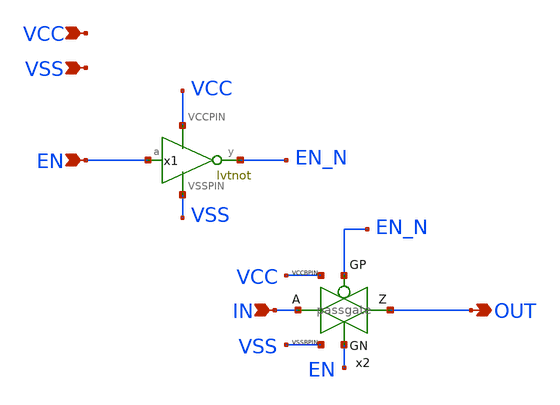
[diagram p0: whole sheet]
** sch_path: xschem/analogswitch.sch
* xschem/lvtnot.sym:
* Copyright 2021 Stefan Frederik Schippers
* Licensed under the Apache License, Version 2.0 (the "License");
**.subckt analogswitch EN IN OUT VCC VSS
*.ipin EN
*.ipin IN
*.opin OUT
*.ipin VCC
*.ipin VSS
x2 OUT IN EN_N EN VSS VCC passgate
x1 EN EN_N VCC VSS lvtnot
**.ends

* expanding   symbol:  passgate.sym # of pins=6
** sym_path: xschem/passgate.sym
** sch_path: xschem/passgate.sch
.subckt passgate Z A GP GN VSSBPIN VCCBPIN
*.iopin A
*.iopin Z
*.ipin GP
*.ipin GN
*.ipin VCCBPIN
*.ipin VSSBPIN
XM1 Z GN A VSSBPIN sky130_fd_pr__nfet_01v8 L=0.2 W=2 nf=1 ad='int((nf+1)/2) * W/nf * 0.29' as='int((nf+2)/2) * W/nf * 0.29'
+ pd='2*int((nf+1)/2) * (W/nf + 0.29)' ps='2*int((nf+2)/2) * (W/nf + 0.29)' nrd='0.29 / W' nrs='0.29 / W'
+ sa=0 sb=0 sd=0 mult=1 m=1
XM2 Z GP A VCCBPIN sky130_fd_pr__pfet_01v8 L=0.2 W=2 nf=1 ad='int((nf+1)/2) * W/nf * 0.29' as='int((nf+2)/2) * W/nf * 0.29'
+ pd='2*int((nf+1)/2) * (W/nf + 0.29)' ps='2*int((nf+2)/2) * (W/nf + 0.29)' nrd='0.29 / W' nrs='0.29 / W'
+ sa=0 sb=0 sd=0 mult=1 m=1
.ends


* expanding   symbol:  lvtnot.sym # of pins=4
** sym_path: xschem/lvtnot.sym
** sch_path: xschem/lvtnot.sch
.subckt lvtnot a y VCCPIN VSSPIN
*.opin y
*.ipin a
*.ipin VCCPIN
*.ipin VSSPIN
XM2 y a VCCPIN VCCPIN sky130_fd_pr__pfet_01v8_lvt L=0.35 W=2 nf=1 ad='int((1 + 1)/2) * 2 / 1 * 0.29'
+ as='int((1 + 2)/2) * 2 / 1 * 0.29' pd='2*int((1 + 1)/2) * (2 / 1 + 0.29)' ps='2*int((1 + 2)/2) * (2 / 1 + 0.29)'
+ nrd='0.29 / 2 ' nrs='0.29 / 2 ' sa=0 sb=0 sd=0 mult=1 m=1
XM1 y a VSSPIN VSSPIN sky130_fd_pr__nfet_01v8_lvt L=0.15 W=1 nf=1 ad='int((1 + 1)/2) * 1 / 1 * 0.29'
+ as='int((1 + 2)/2) * 1 / 1 * 0.29' pd='2*int((1 + 1)/2) * (1 / 1 + 0.29)' ps='2*int((1 + 2)/2) * (1 / 1 + 0.29)'
+ nrd='0.29 / 1 ' nrs='0.29 / 1 ' sa=0 sb=0 sd=0 mult=1 m=1
.ends

.end
